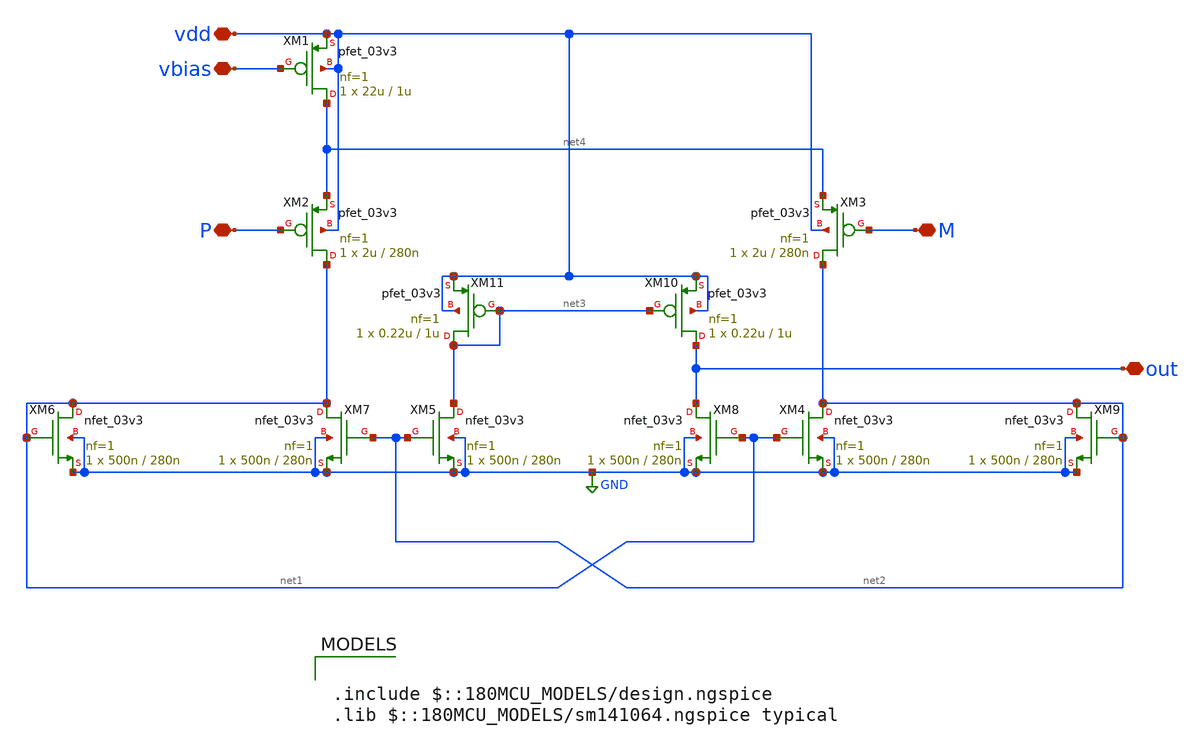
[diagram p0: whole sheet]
** sch_path: Clock_Reference/symbols/comparator.sch
**.subckt comparator out M P vbias vdd
*.iopin out
*.iopin M
*.iopin P
*.iopin vbias
*.iopin vdd
XM1 net4 vbias vdd vdd pfet_03v3 L=1u W=22u nf=1 ad='int((nf+1)/2) * W/nf * 0.18u' as='int((nf+2)/2) * W/nf * 0.18u'
+ pd='2*int((nf+1)/2) * (W/nf + 0.18u)' ps='2*int((nf+2)/2) * (W/nf + 0.18u)' nrd='0.18u / W' nrs='0.18u / W'
+ sa=0 sb=0 sd=0 m=1
XM2 net1 P net4 vdd pfet_03v3 L=280n W=2u nf=1 ad='int((nf+1)/2) * W/nf * 0.18u' as='int((nf+2)/2) * W/nf * 0.18u'
+ pd='2*int((nf+1)/2) * (W/nf + 0.18u)' ps='2*int((nf+2)/2) * (W/nf + 0.18u)' nrd='0.18u / W' nrs='0.18u / W'
+ sa=0 sb=0 sd=0 m=1
XM3 net2 M net4 vdd pfet_03v3 L=280n W=2u nf=1 ad='int((nf+1)/2) * W/nf * 0.18u' as='int((nf+2)/2) * W/nf * 0.18u'
+ pd='2*int((nf+1)/2) * (W/nf + 0.18u)' ps='2*int((nf+2)/2) * (W/nf + 0.18u)' nrd='0.18u / W' nrs='0.18u / W'
+ sa=0 sb=0 sd=0 m=1
XM4 net2 net1 GND GND nfet_03v3 L=280n W=500n nf=1 ad='int((nf+1)/2) * W/nf * 0.18u' as='int((nf+2)/2) * W/nf * 0.18u'
+ pd='2*int((nf+1)/2) * (W/nf + 0.18u)' ps='2*int((nf+2)/2) * (W/nf + 0.18u)' nrd='0.18u / W' nrs='0.18u / W'
+ sa=0 sb=0 sd=0 m=1
XM5 net3 net2 GND GND nfet_03v3 L=280n W=500n nf=1 ad='int((nf+1)/2) * W/nf * 0.18u' as='int((nf+2)/2) * W/nf * 0.18u'
+ pd='2*int((nf+1)/2) * (W/nf + 0.18u)' ps='2*int((nf+2)/2) * (W/nf + 0.18u)' nrd='0.18u / W' nrs='0.18u / W'
+ sa=0 sb=0 sd=0 m=1
XM6 net1 net1 GND GND nfet_03v3 L=280n W=500n nf=1 ad='int((nf+1)/2) * W/nf * 0.18u' as='int((nf+2)/2) * W/nf * 0.18u'
+ pd='2*int((nf+1)/2) * (W/nf + 0.18u)' ps='2*int((nf+2)/2) * (W/nf + 0.18u)' nrd='0.18u / W' nrs='0.18u / W'
+ sa=0 sb=0 sd=0 m=1
XM7 net1 net2 GND GND nfet_03v3 L=280n W=500n nf=1 ad='int((nf+1)/2) * W/nf * 0.18u' as='int((nf+2)/2) * W/nf * 0.18u'
+ pd='2*int((nf+1)/2) * (W/nf + 0.18u)' ps='2*int((nf+2)/2) * (W/nf + 0.18u)' nrd='0.18u / W' nrs='0.18u / W'
+ sa=0 sb=0 sd=0 m=1
XM8 out net1 GND GND nfet_03v3 L=280n W=500n nf=1 ad='int((nf+1)/2) * W/nf * 0.18u' as='int((nf+2)/2) * W/nf * 0.18u'
+ pd='2*int((nf+1)/2) * (W/nf + 0.18u)' ps='2*int((nf+2)/2) * (W/nf + 0.18u)' nrd='0.18u / W' nrs='0.18u / W'
+ sa=0 sb=0 sd=0 m=1
XM9 net2 net2 GND GND nfet_03v3 L=280n W=500n nf=1 ad='int((nf+1)/2) * W/nf * 0.18u' as='int((nf+2)/2) * W/nf * 0.18u'
+ pd='2*int((nf+1)/2) * (W/nf + 0.18u)' ps='2*int((nf+2)/2) * (W/nf + 0.18u)' nrd='0.18u / W' nrs='0.18u / W'
+ sa=0 sb=0 sd=0 m=1
XM10 out net3 vdd vdd pfet_03v3 L=1u W=0.22u nf=1 ad='int((nf+1)/2) * W/nf * 0.18u' as='int((nf+2)/2) * W/nf * 0.18u'
+ pd='2*int((nf+1)/2) * (W/nf + 0.18u)' ps='2*int((nf+2)/2) * (W/nf + 0.18u)' nrd='0.18u / W' nrs='0.18u / W'
+ sa=0 sb=0 sd=0 m=1
XM11 net3 net3 vdd vdd pfet_03v3 L=1u W=0.22u nf=1 ad='int((nf+1)/2) * W/nf * 0.18u' as='int((nf+2)/2) * W/nf * 0.18u'
+ pd='2*int((nf+1)/2) * (W/nf + 0.18u)' ps='2*int((nf+2)/2) * (W/nf + 0.18u)' nrd='0.18u / W' nrs='0.18u / W'
+ sa=0 sb=0 sd=0 m=1
**** begin user architecture code

.include $::180MCU_MODELS/design.ngspice
.lib $::180MCU_MODELS/sm141064.ngspice typical

**** end user architecture code
**.ends
.GLOBAL GND
.end
